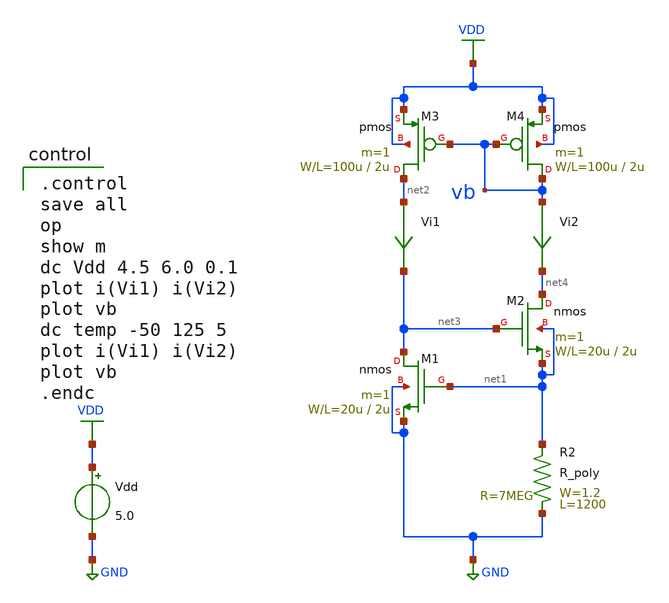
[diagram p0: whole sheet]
** sch_path: OR1/PTC06/current-source/cs-vth-ref.sch
**.subckt cs-vth-ref
Vdd VDD GND 5.0
Vi1 net2 net3 0
.save i(vi1)
Vi2 vb net4 0
.save i(vi2)
R2 GND net1 R_poly W=1.2 L=1200
M4 vb vb VDD VDD pmos L=2u W=100u m=1
M3 net2 vb VDD VDD pmos L=2u W=100u m=1
M2 net4 net3 net1 net1 nmos L=2u W=20u m=1
M1 net3 net1 GND GND nmos L=2u W=20u m=1
**** begin user architecture code

.control
save all
op
show m
dc Vdd 4.5 6.0 0.1
plot i(Vi1) i(Vi2)
plot vb
dc temp -50 125 5
plot i(Vi1) i(Vi2)
plot vb
.endc

 .include $::LIB/mos.lib
.include $::LIB/passive.lib
.include $::LIB/diode.lib
**** end user architecture code
**.ends
.GLOBAL GND
.GLOBAL VDD
.end
